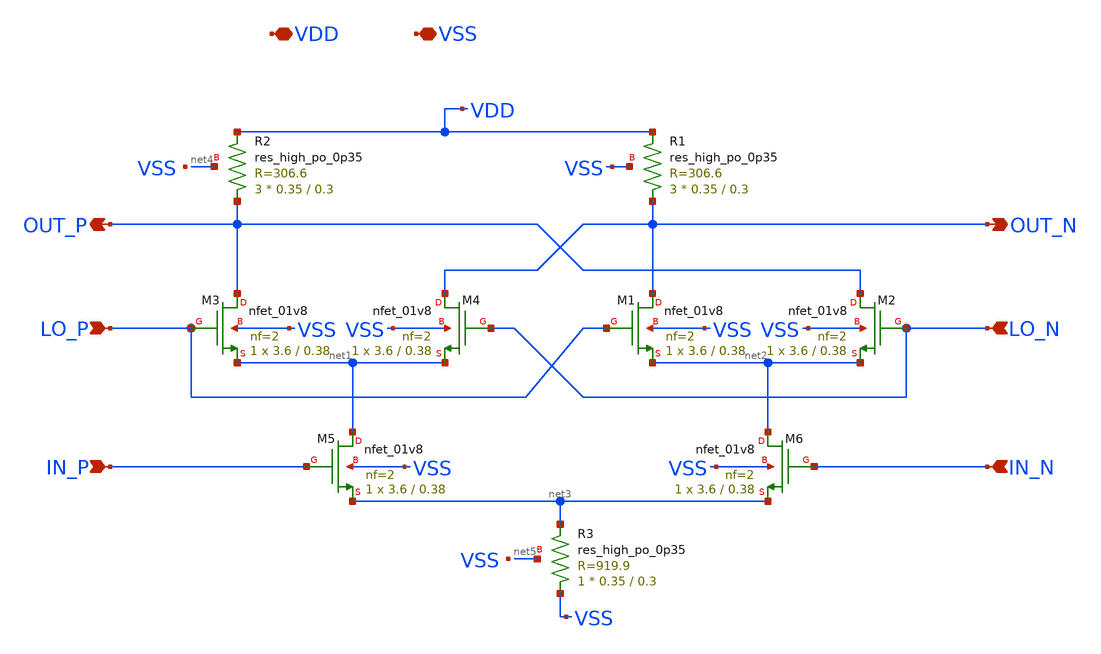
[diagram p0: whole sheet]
** sch_path: xschem/gilbert_mixer.sch
**.subckt gilbert_mixer VDD VSS LO_P LO_N IN_P IN_N OUT_N OUT_P
*.iopin VDD
*.iopin VSS
*.ipin LO_P
*.ipin LO_N
*.ipin IN_P
*.ipin IN_N
*.opin OUT_N
*.opin OUT_P
XR3 VSS net3 net5 sky130_fd_pr__res_high_po_0p35 L=0.3 mult=1 m=1
XM2 OUT_P LO_N net2 VSS sky130_fd_pr__nfet_01v8 L=0.38 W=3.6 nf=2 ad='int((nf+1)/2) * W/nf * 0.29' as='int((nf+2)/2) * W/nf * 0.29'
+ pd='2*int((nf+1)/2) * (W/nf + 0.29)' ps='2*int((nf+2)/2) * (W/nf + 0.29)' nrd='0.29 / W' nrs='0.29 / W'
+ sa=0 sb=0 sd=0 mult=1 m=1
XM4 OUT_N LO_N net1 VSS sky130_fd_pr__nfet_01v8 L=0.38 W=3.6 nf=2 ad='int((nf+1)/2) * W/nf * 0.29' as='int((nf+2)/2) * W/nf * 0.29'
+ pd='2*int((nf+1)/2) * (W/nf + 0.29)' ps='2*int((nf+2)/2) * (W/nf + 0.29)' nrd='0.29 / W' nrs='0.29 / W'
+ sa=0 sb=0 sd=0 mult=1 m=1
XM6 net2 IN_N net3 VSS sky130_fd_pr__nfet_01v8 L=0.38 W=3.6 nf=2 ad='int((nf+1)/2) * W/nf * 0.29' as='int((nf+2)/2) * W/nf * 0.29'
+ pd='2*int((nf+1)/2) * (W/nf + 0.29)' ps='2*int((nf+2)/2) * (W/nf + 0.29)' nrd='0.29 / W' nrs='0.29 / W'
+ sa=0 sb=0 sd=0 mult=1 m=1
XM1 OUT_N LO_P net2 VSS sky130_fd_pr__nfet_01v8 L=0.38 W=3.6 nf=2 ad='int((nf+1)/2) * W/nf * 0.29' as='int((nf+2)/2) * W/nf * 0.29'
+ pd='2*int((nf+1)/2) * (W/nf + 0.29)' ps='2*int((nf+2)/2) * (W/nf + 0.29)' nrd='0.29 / W' nrs='0.29 / W'
+ sa=0 sb=0 sd=0 mult=1 m=1
XM3 OUT_P LO_P net1 VSS sky130_fd_pr__nfet_01v8 L=0.38 W=3.6 nf=2 ad='int((nf+1)/2) * W/nf * 0.29' as='int((nf+2)/2) * W/nf * 0.29'
+ pd='2*int((nf+1)/2) * (W/nf + 0.29)' ps='2*int((nf+2)/2) * (W/nf + 0.29)' nrd='0.29 / W' nrs='0.29 / W'
+ sa=0 sb=0 sd=0 mult=1 m=1
XM5 net1 IN_P net3 VSS sky130_fd_pr__nfet_01v8 L=0.38 W=3.6 nf=2 ad='int((nf+1)/2) * W/nf * 0.29' as='int((nf+2)/2) * W/nf * 0.29'
+ pd='2*int((nf+1)/2) * (W/nf + 0.29)' ps='2*int((nf+2)/2) * (W/nf + 0.29)' nrd='0.29 / W' nrs='0.29 / W'
+ sa=0 sb=0 sd=0 mult=1 m=1
XR1 OUT_N VDD VSS sky130_fd_pr__res_high_po_0p35 L=0.3 mult=3 m=3
XR2 OUT_P VDD net4 sky130_fd_pr__res_high_po_0p35 L=0.3 mult=3 m=3
**.ends
.end
